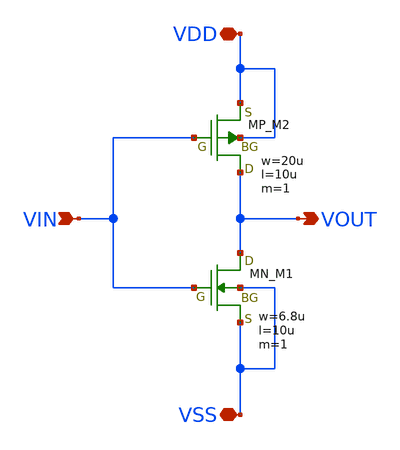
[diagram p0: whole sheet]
** sch_path: member_project/JJY_Receiver/Masahiro/jjy_recv/pre_amp/inverter.sch
**.subckt inverter VIN VOUT VSS VDD
*.ipin VIN
*.opin VOUT
*.iopin VSS
*.iopin VDD
XM1 VOUT VIN VSS VSS NMOS w=6.8u l=10u as=0 ad=0 ps=0 pd=0 nrd=0 nrs=0 m=1
XM2 VOUT VIN VDD VDD PMOS w=20u l=10u as=0 ad=0 ps=0 pd=0 nrd=0 nrs=0 m=1
**** begin user architecture code
 .include $::LIB/ip62_models
**** end user architecture code
**.ends
.end
